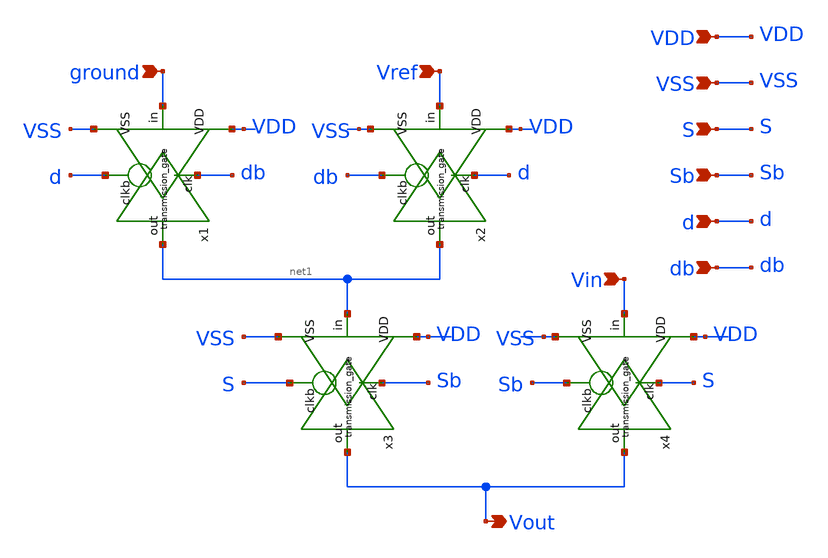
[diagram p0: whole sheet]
** sch_path: Network_Switch.sch
**.subckt Network_Switch ground Vref Vin Vout VDD VSS S Sb d db
*.ipin ground
*.ipin Vref
*.ipin Vin
*.opin Vout
*.ipin VDD
*.ipin VSS
*.ipin S
*.ipin Sb
*.ipin d
*.ipin db
x1 ground d db VDD VSS net1 transmission_gate
x2 Vref db d VDD VSS net1 transmission_gate
x3 net1 S Sb VDD VSS Vout transmission_gate
x4 Vin Sb S VDD VSS Vout transmission_gate
**.ends

* expanding   symbol:  transmission_gate.sym # of pins=6
** sym_path: transmission_gate.sym
** sch_path: transmission_gate.sch
.subckt transmission_gate in clkb clk VDD VSS out
*.ipin in
*.ipin clk
*.ipin clkb
*.opin out
*.ipin VDD
*.ipin VSS
XM1 out clk in VSS sky130_fd_pr__nfet_01v8 L=0.15 W=0.5 nf=1 ad='int((nf+1)/2) * W/nf * 0.29' as='int((nf+2)/2) * W/nf * 0.29'
+ pd='2*int((nf+1)/2) * (W/nf + 0.29)' ps='2*int((nf+2)/2) * (W/nf + 0.29)' nrd='0.29 / W' nrs='0.29 / W'
+ sa=0 sb=0 sd=0 mult=1 m=1
XM2 out clkb in VDD sky130_fd_pr__pfet_01v8 L=0.15 W=0.5 nf=1 ad='int((nf+1)/2) * W/nf * 0.29' as='int((nf+2)/2) * W/nf * 0.29'
+ pd='2*int((nf+1)/2) * (W/nf + 0.29)' ps='2*int((nf+2)/2) * (W/nf + 0.29)' nrd='0.29 / W' nrs='0.29 / W'
+ sa=0 sb=0 sd=0 mult=1 m=1
.ends

.end
